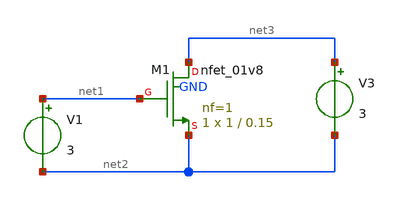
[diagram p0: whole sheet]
** sch_path: test_xschem_sky130/FET_test.sch
**.subckt FET_test
XM1 net3 net1 net2 GND sky130_fd_pr__nfet_01v8 L=0.15 W=1 nf=1 ad='int((1 + 1)/2) * 1 / 1 * 0.29' as='int((1 + 2)/2) * 1 / 1 * 0.29'
+ pd='2*int((1 + 1)/2) * (1 / 1 + 0.29)' ps='2*int((1 + 2)/2) * (1 / 1 + 0.29)' nrd='0.29 / 1 ' nrs='0.29 / 1 '
+ sa=0 sb=0 sd=0 mult=1 m=1
V1 net1 net2 3
V3 net3 net2 3
**.ends
.end
